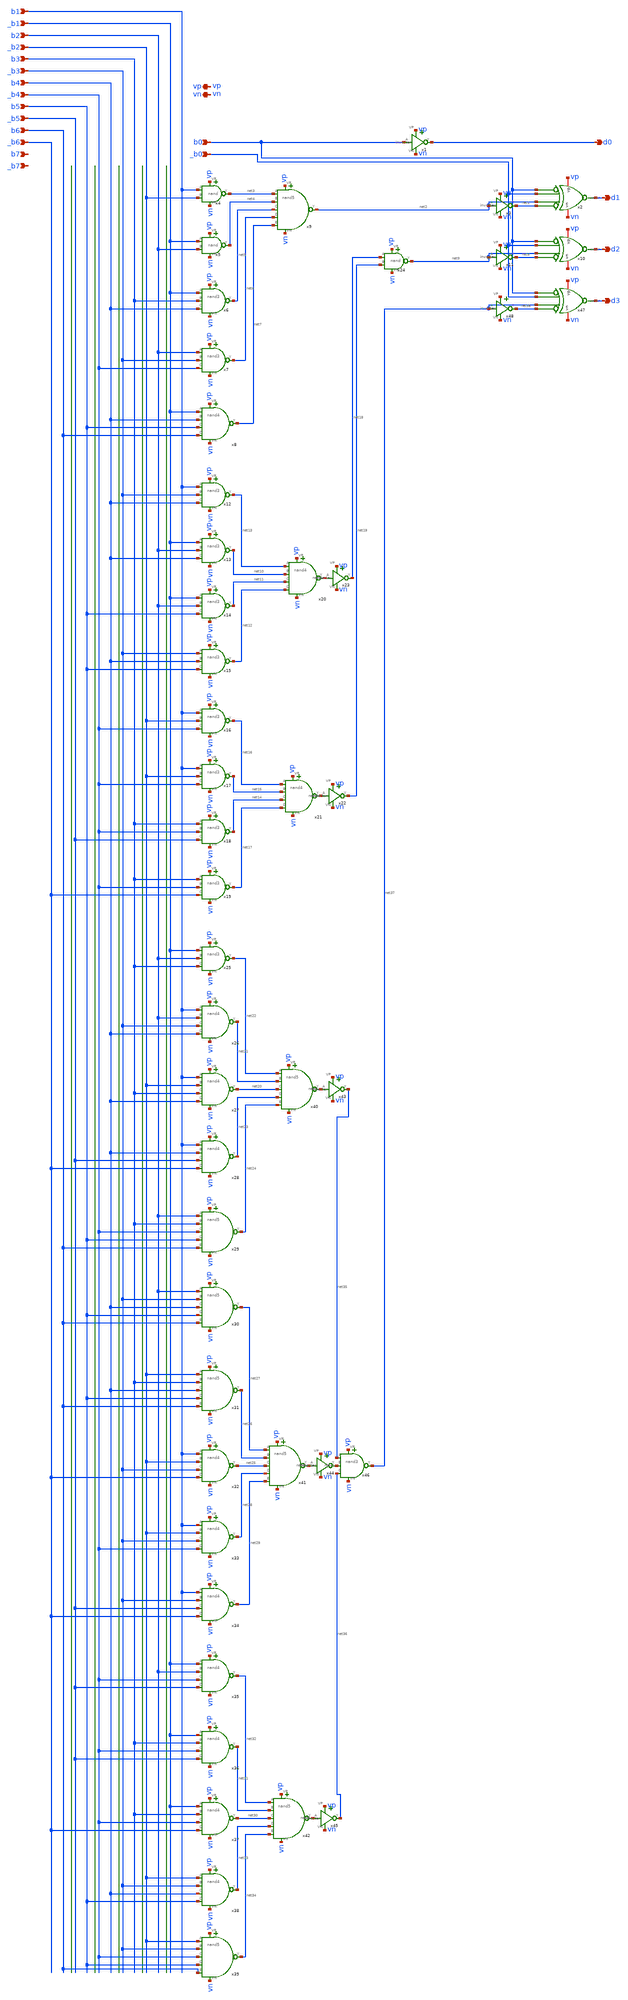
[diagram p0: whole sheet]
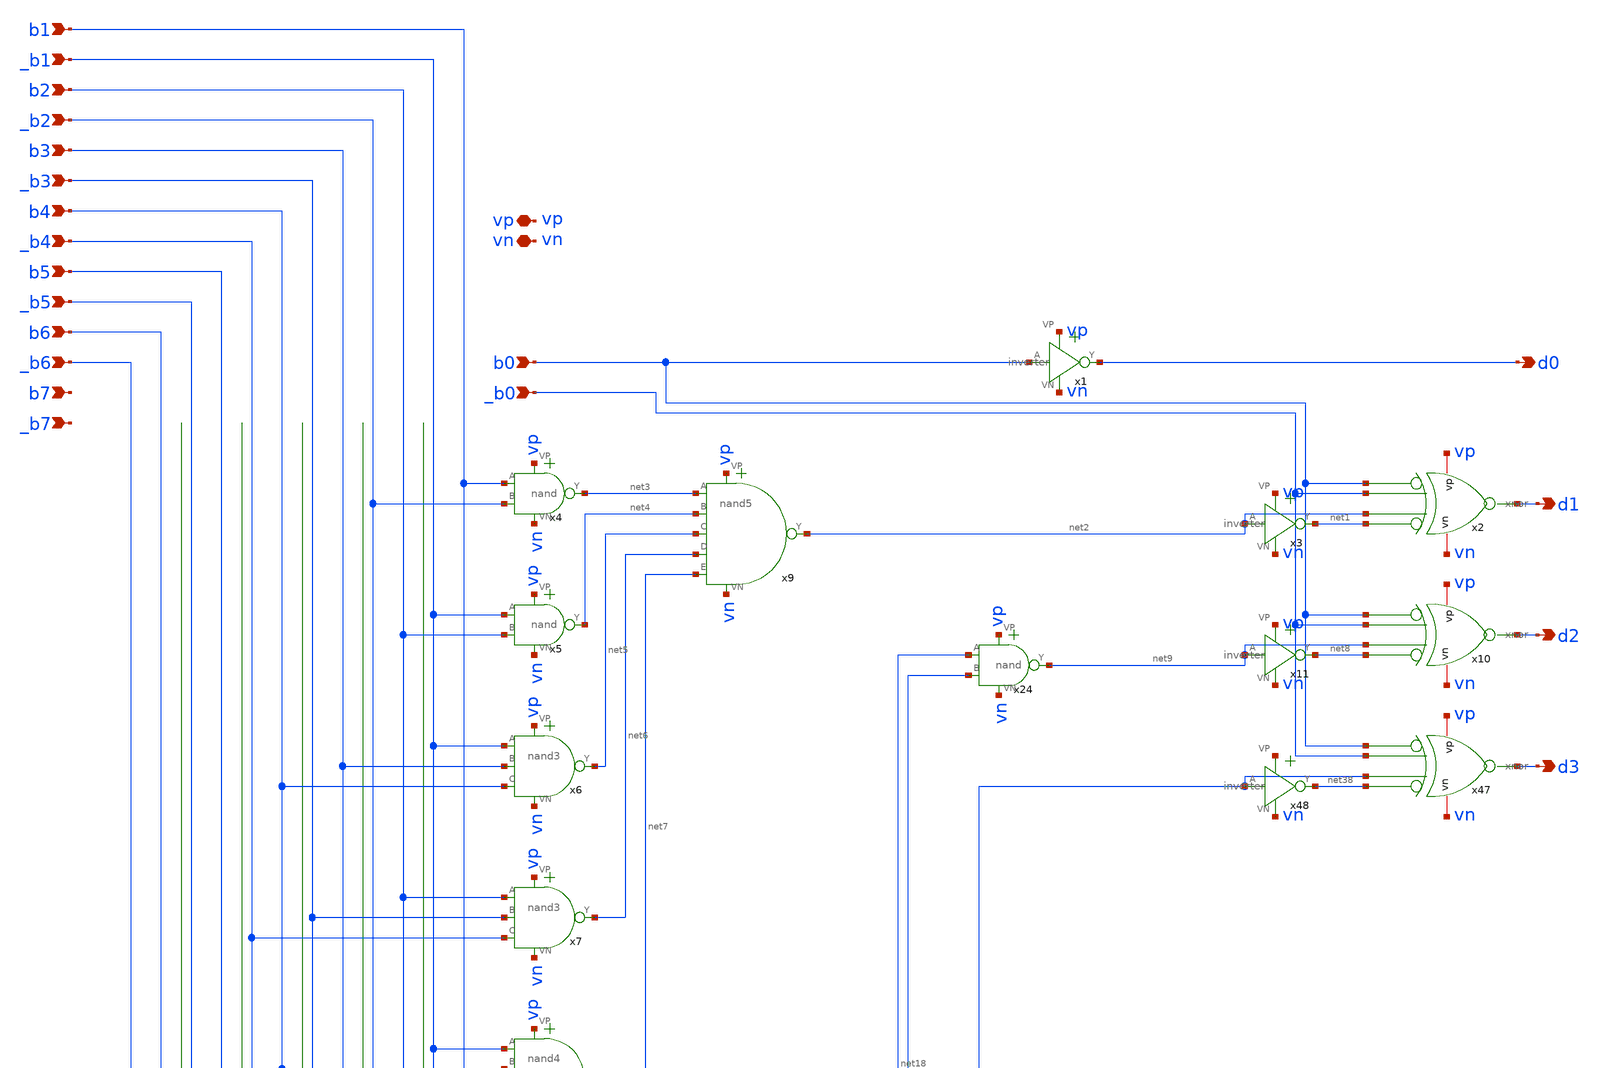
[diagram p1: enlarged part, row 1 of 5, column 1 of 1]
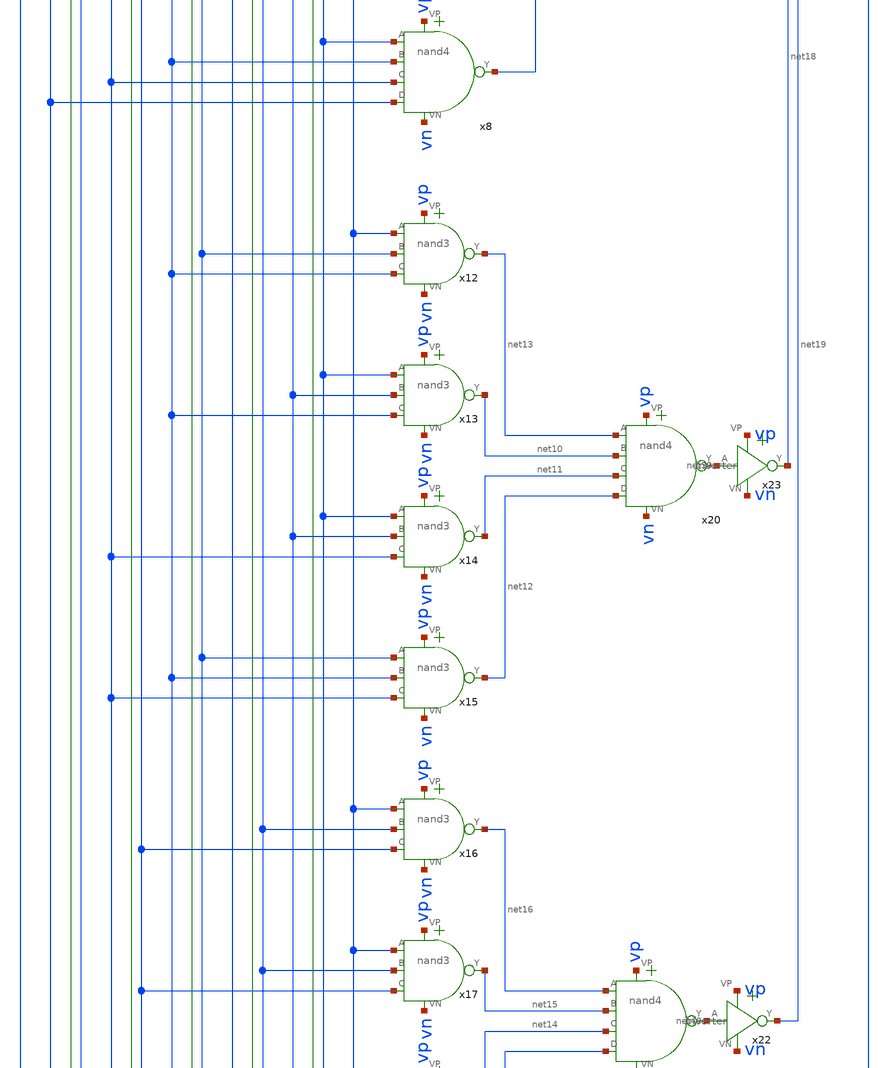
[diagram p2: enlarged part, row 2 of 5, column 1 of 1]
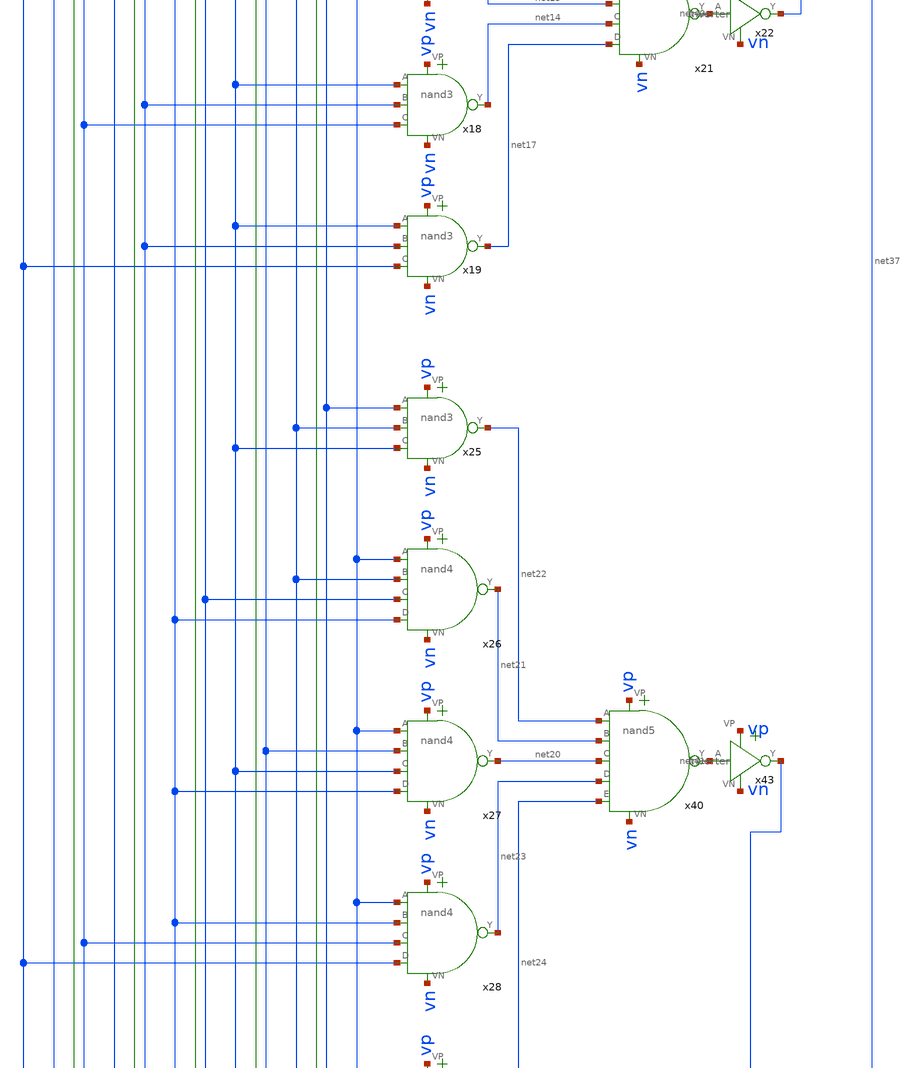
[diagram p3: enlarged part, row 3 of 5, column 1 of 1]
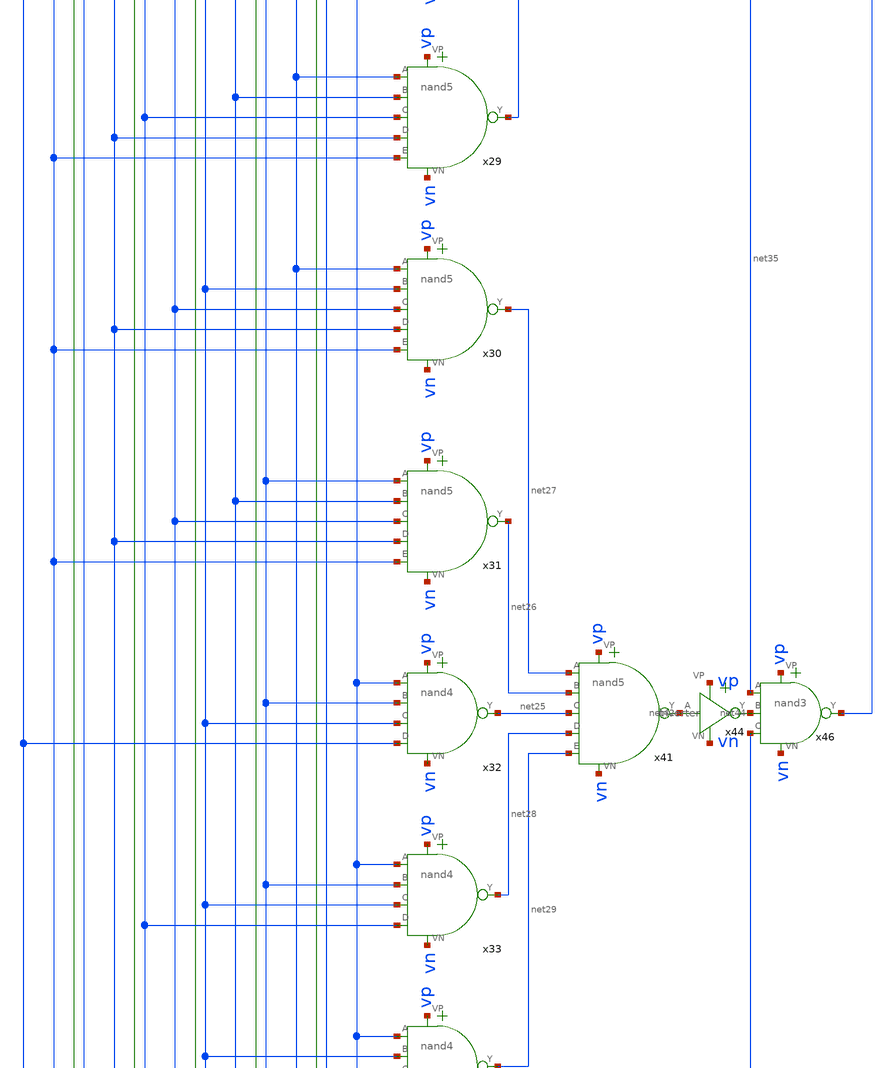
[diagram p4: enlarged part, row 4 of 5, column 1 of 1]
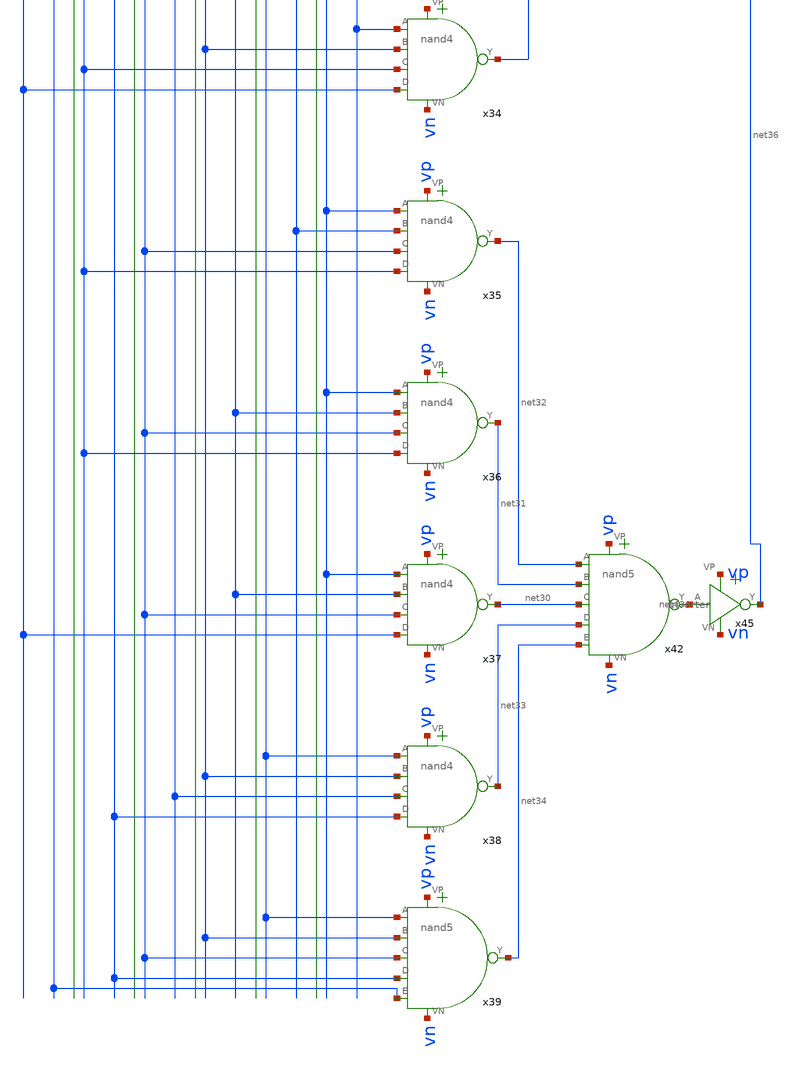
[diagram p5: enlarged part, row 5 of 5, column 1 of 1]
** sch_path: xschem/sin_cl.sch
**.subckt sin_cl _b0 b1 _b1 b2 _b2 b3 _b3 b4 _b4 b5 _b5 b6 _b6 b7 _b7 b0 d0 d1 d2 d3 vp vn
*.ipin _b0
*.ipin b1
*.ipin _b1
*.ipin b2
*.ipin _b2
*.ipin b3
*.ipin _b3
*.ipin b4
*.ipin _b4
*.ipin b5
*.ipin _b5
*.ipin b6
*.ipin _b6
*.ipin b7
*.ipin _b7
*.ipin b0
*.opin d0
*.opin d1
*.opin d2
*.opin d3
*.iopin vp
*.iopin vn
x1 vp b0 d0 vn inverter
x2 vp _b0 net2 d1 b0 net1 vn xnor
x3 vp net2 net1 vn inverter
x4 vn b1 _b2 net3 vp nand
x5 vn _b1 b2 net4 vp nand
x6 vn _b1 b3 net5 vp b4 nand3
x7 vn b2 _b3 net6 vp _b4 nand3
x8 vn _b1 b4 net7 vp b5 b6 nand4
x9 vn net3 net4 net2 vp net5 net6 net7 nand5
x10 vp _b0 net9 d2 b0 net8 vn xnor
x11 vp net9 net8 vn inverter
x12 vn b1 _b3 net13 vp b4 nand3
x13 vn _b1 b2 net10 vp b4 nand3
x14 vn _b1 b2 net11 vp b5 nand3
x15 vn _b3 b4 net12 vp b5 nand3
x16 vn b1 _b2 net16 vp _b4 nand3
x17 vn b1 _b2 net15 vp _b4 nand3
x18 vn b3 _b4 net14 vp _b5 nand3
x19 vn b3 _b4 net17 vp _b6 nand3
x20 vn net13 net10 net39 vp net11 net12 nand4
x21 vn net16 net15 net40 vp net14 net17 nand4
x22 vp net40 net19 vn inverter
x23 vp net39 net18 vn inverter
x24 vn net18 net19 net9 vp nand
x25 vn _b1 b2 net22 vp b3 nand3
x26 vn b1 b2 net21 vp _b3 b4 nand4
x27 vn b1 _b2 net20 vp b3 b4 nand4
x28 vn b1 b4 net23 vp _b5 _b6 nand4
x29 vn b2 b3 net24 vp _b4 b5 b6 nand5
x30 vn b2 _b3 net27 vp b4 b5 b6 nand5
x31 vn _b2 b3 net26 vp b4 b5 b6 nand5
x32 vn b1 _b2 net25 vp _b3 _b6 nand4
x33 vn b1 _b2 net28 vp _b3 _b4 nand4
x34 vn b1 _b3 net29 vp _b5 _b6 nand4
x35 vn _b1 b2 net32 vp _b4 _b5 nand4
x36 vn _b1 b3 net31 vp _b4 _b5 nand4
x37 vn _b1 b3 net30 vp _b4 _b6 nand4
x38 vn _b2 _b3 net33 vp b4 b5 nand4
x39 vn _b2 _b3 net34 vp _b4 b5 b6 nand5
x40 vn net22 net21 net41 vp net20 net23 net24 nand5
x41 vn net27 net26 net42 vp net25 net28 net29 nand5
x42 vn net32 net31 net43 vp net30 net33 net34 nand5
x43 vp net41 net35 vn inverter
x44 vp net42 net44 vn inverter
x45 vp net43 net36 vn inverter
x46 vn net35 net44 net37 vp net36 nand3
x47 vp _b0 net37 d3 b0 net38 vn xnor
x48 net45 net37 net38 vn inverter
**.ends

* expanding   symbol:  /home/madvlsi/dev/git/magic-dds/xschem/other_project_files/inverter.sym # of
*+ pins=4
** sym_path: xschem/other_project_files/inverter.sym
** sch_path: xschem/other_project_files/inverter.sch
.subckt inverter VP A Y VN
*.iopin VP
*.iopin VN
*.ipin A
*.opin Y
XM1 Y A VN VN sky130_fd_pr__nfet_01v8 L=0.15 W=1 nf=1 ad='int((nf+1)/2) * W/nf * 0.29' as='int((nf+2)/2) * W/nf * 0.29'
+ pd='2*int((nf+1)/2) * (W/nf + 0.29)' ps='2*int((nf+2)/2) * (W/nf + 0.29)' nrd='0.29 / W' nrs='0.29 / W'
+ sa=0 sb=0 sd=0 mult=1 m=1
XM2 Y A VP VP sky130_fd_pr__pfet_01v8 L=0.15 W=4 nf=1 ad='int((nf+1)/2) * W/nf * 0.29' as='int((nf+2)/2) * W/nf * 0.29'
+ pd='2*int((nf+1)/2) * (W/nf + 0.29)' ps='2*int((nf+2)/2) * (W/nf + 0.29)' nrd='0.29 / W' nrs='0.29 / W'
+ sa=0 sb=0 sd=0 mult=1 m=1
.ends


* expanding   symbol:  /home/madvlsi/dev/git/magic-dds/xschem/logic_gates/xnor.sym # of pins=7
** sym_path: xschem/logic_gates/xnor.sym
** sch_path: xschem/logic_gates/xnor.sch
.subckt xnor vp A B Y _A _B vn
*.iopin vp
*.iopin vn
*.ipin A
*.ipin B
*.ipin _A
*.ipin _B
*.opin Y
x1 vn A B net1 vp nand
x2 vn _A _B net2 vp nand
x3 vn net1 net2 Y vp nand
.ends


* expanding   symbol:  /home/madvlsi/dev/git/magic-dds/xschem/logic_gates/nand.sym # of pins=5
** sym_path: xschem/logic_gates/nand.sym
** sch_path: xschem/logic_gates/nand.sch
.subckt nand VN A B Y VP
*.iopin VP
*.iopin VN
*.ipin A
*.ipin B
*.opin Y
XM1 Y A net1 GND sky130_fd_pr__nfet_01v8 L=0.15 W=1 nf=1 ad='int((nf+1)/2) * W/nf * 0.29' as='int((nf+2)/2) * W/nf * 0.29'
+ pd='2*int((nf+1)/2) * (W/nf + 0.29)' ps='2*int((nf+2)/2) * (W/nf + 0.29)' nrd='0.29 / W' nrs='0.29 / W'
+ sa=0 sb=0 sd=0 mult=1 m=1
XM2 net1 B VN GND sky130_fd_pr__nfet_01v8 L=0.15 W=1 nf=1 ad='int((nf+1)/2) * W/nf * 0.29' as='int((nf+2)/2) * W/nf * 0.29'
+ pd='2*int((nf+1)/2) * (W/nf + 0.29)' ps='2*int((nf+2)/2) * (W/nf + 0.29)' nrd='0.29 / W' nrs='0.29 / W'
+ sa=0 sb=0 sd=0 mult=1 m=1
XM3 Y A VP VDD sky130_fd_pr__pfet_01v8 L=0.15 W=1 nf=1 ad='int((nf+1)/2) * W/nf * 0.29' as='int((nf+2)/2) * W/nf * 0.29'
+ pd='2*int((nf+1)/2) * (W/nf + 0.29)' ps='2*int((nf+2)/2) * (W/nf + 0.29)' nrd='0.29 / W' nrs='0.29 / W'
+ sa=0 sb=0 sd=0 mult=1 m=1
XM4 Y B VP VDD sky130_fd_pr__pfet_01v8 L=0.15 W=1 nf=1 ad='int((nf+1)/2) * W/nf * 0.29' as='int((nf+2)/2) * W/nf * 0.29'
+ pd='2*int((nf+1)/2) * (W/nf + 0.29)' ps='2*int((nf+2)/2) * (W/nf + 0.29)' nrd='0.29 / W' nrs='0.29 / W'
+ sa=0 sb=0 sd=0 mult=1 m=1
.ends


* expanding   symbol:  /home/madvlsi/dev/git/magic-dds/xschem/logic_gates/nand3.sym # of pins=6
** sym_path: xschem/logic_gates/nand3.sym
** sch_path: xschem/logic_gates/nand3.sch
.subckt nand3 VN A B Y VP C
*.iopin VP
*.iopin VN
*.ipin A
*.ipin B
*.opin Y
*.ipin C
XM1 Y A net1 GND sky130_fd_pr__nfet_01v8 L=0.15 W=1 nf=1 ad='int((nf+1)/2) * W/nf * 0.29' as='int((nf+2)/2) * W/nf * 0.29'
+ pd='2*int((nf+1)/2) * (W/nf + 0.29)' ps='2*int((nf+2)/2) * (W/nf + 0.29)' nrd='0.29 / W' nrs='0.29 / W'
+ sa=0 sb=0 sd=0 mult=1 m=1
XM2 net1 B net2 GND sky130_fd_pr__nfet_01v8 L=0.15 W=1 nf=1 ad='int((nf+1)/2) * W/nf * 0.29' as='int((nf+2)/2) * W/nf * 0.29'
+ pd='2*int((nf+1)/2) * (W/nf + 0.29)' ps='2*int((nf+2)/2) * (W/nf + 0.29)' nrd='0.29 / W' nrs='0.29 / W'
+ sa=0 sb=0 sd=0 mult=1 m=1
XM3 Y A VP VDD sky130_fd_pr__pfet_01v8 L=0.15 W=1 nf=1 ad='int((nf+1)/2) * W/nf * 0.29' as='int((nf+2)/2) * W/nf * 0.29'
+ pd='2*int((nf+1)/2) * (W/nf + 0.29)' ps='2*int((nf+2)/2) * (W/nf + 0.29)' nrd='0.29 / W' nrs='0.29 / W'
+ sa=0 sb=0 sd=0 mult=1 m=1
XM4 Y B VP VDD sky130_fd_pr__pfet_01v8 L=0.15 W=1 nf=1 ad='int((nf+1)/2) * W/nf * 0.29' as='int((nf+2)/2) * W/nf * 0.29'
+ pd='2*int((nf+1)/2) * (W/nf + 0.29)' ps='2*int((nf+2)/2) * (W/nf + 0.29)' nrd='0.29 / W' nrs='0.29 / W'
+ sa=0 sb=0 sd=0 mult=1 m=1
XM5 net2 C VN GND sky130_fd_pr__nfet_01v8 L=0.15 W=1 nf=1 ad='int((nf+1)/2) * W/nf * 0.29' as='int((nf+2)/2) * W/nf * 0.29'
+ pd='2*int((nf+1)/2) * (W/nf + 0.29)' ps='2*int((nf+2)/2) * (W/nf + 0.29)' nrd='0.29 / W' nrs='0.29 / W'
+ sa=0 sb=0 sd=0 mult=1 m=1
XM6 Y C VP VDD sky130_fd_pr__pfet_01v8 L=0.15 W=1 nf=1 ad='int((nf+1)/2) * W/nf * 0.29' as='int((nf+2)/2) * W/nf * 0.29'
+ pd='2*int((nf+1)/2) * (W/nf + 0.29)' ps='2*int((nf+2)/2) * (W/nf + 0.29)' nrd='0.29 / W' nrs='0.29 / W'
+ sa=0 sb=0 sd=0 mult=1 m=1
.ends


* expanding   symbol:  /home/madvlsi/dev/git/magic-dds/xschem/logic_gates/nand4.sym # of pins=7
** sym_path: xschem/logic_gates/nand4.sym
** sch_path: xschem/logic_gates/nand4.sch
.subckt nand4 VN A B Y VP C D
*.iopin VP
*.iopin VN
*.ipin A
*.ipin B
*.opin Y
*.ipin C
*.ipin D
XM1 Y A net1 GND sky130_fd_pr__nfet_01v8 L=0.15 W=1 nf=1 ad='int((nf+1)/2) * W/nf * 0.29' as='int((nf+2)/2) * W/nf * 0.29'
+ pd='2*int((nf+1)/2) * (W/nf + 0.29)' ps='2*int((nf+2)/2) * (W/nf + 0.29)' nrd='0.29 / W' nrs='0.29 / W'
+ sa=0 sb=0 sd=0 mult=1 m=1
XM2 net1 B net2 GND sky130_fd_pr__nfet_01v8 L=0.15 W=1 nf=1 ad='int((nf+1)/2) * W/nf * 0.29' as='int((nf+2)/2) * W/nf * 0.29'
+ pd='2*int((nf+1)/2) * (W/nf + 0.29)' ps='2*int((nf+2)/2) * (W/nf + 0.29)' nrd='0.29 / W' nrs='0.29 / W'
+ sa=0 sb=0 sd=0 mult=1 m=1
XM3 Y A VP VDD sky130_fd_pr__pfet_01v8 L=0.15 W=1 nf=1 ad='int((nf+1)/2) * W/nf * 0.29' as='int((nf+2)/2) * W/nf * 0.29'
+ pd='2*int((nf+1)/2) * (W/nf + 0.29)' ps='2*int((nf+2)/2) * (W/nf + 0.29)' nrd='0.29 / W' nrs='0.29 / W'
+ sa=0 sb=0 sd=0 mult=1 m=1
XM4 Y B VP VDD sky130_fd_pr__pfet_01v8 L=0.15 W=1 nf=1 ad='int((nf+1)/2) * W/nf * 0.29' as='int((nf+2)/2) * W/nf * 0.29'
+ pd='2*int((nf+1)/2) * (W/nf + 0.29)' ps='2*int((nf+2)/2) * (W/nf + 0.29)' nrd='0.29 / W' nrs='0.29 / W'
+ sa=0 sb=0 sd=0 mult=1 m=1
XM5 net2 C net3 GND sky130_fd_pr__nfet_01v8 L=0.15 W=1 nf=1 ad='int((nf+1)/2) * W/nf * 0.29' as='int((nf+2)/2) * W/nf * 0.29'
+ pd='2*int((nf+1)/2) * (W/nf + 0.29)' ps='2*int((nf+2)/2) * (W/nf + 0.29)' nrd='0.29 / W' nrs='0.29 / W'
+ sa=0 sb=0 sd=0 mult=1 m=1
XM6 Y C VP VDD sky130_fd_pr__pfet_01v8 L=0.15 W=1 nf=1 ad='int((nf+1)/2) * W/nf * 0.29' as='int((nf+2)/2) * W/nf * 0.29'
+ pd='2*int((nf+1)/2) * (W/nf + 0.29)' ps='2*int((nf+2)/2) * (W/nf + 0.29)' nrd='0.29 / W' nrs='0.29 / W'
+ sa=0 sb=0 sd=0 mult=1 m=1
XM7 Y D VP VDD sky130_fd_pr__pfet_01v8 L=0.15 W=1 nf=1 ad='int((nf+1)/2) * W/nf * 0.29' as='int((nf+2)/2) * W/nf * 0.29'
+ pd='2*int((nf+1)/2) * (W/nf + 0.29)' ps='2*int((nf+2)/2) * (W/nf + 0.29)' nrd='0.29 / W' nrs='0.29 / W'
+ sa=0 sb=0 sd=0 mult=1 m=1
XM8 net3 D VN GND sky130_fd_pr__nfet_01v8 L=0.15 W=1 nf=1 ad='int((nf+1)/2) * W/nf * 0.29' as='int((nf+2)/2) * W/nf * 0.29'
+ pd='2*int((nf+1)/2) * (W/nf + 0.29)' ps='2*int((nf+2)/2) * (W/nf + 0.29)' nrd='0.29 / W' nrs='0.29 / W'
+ sa=0 sb=0 sd=0 mult=1 m=1
.ends


* expanding   symbol:  /home/madvlsi/dev/git/magic-dds/xschem/logic_gates/nand5.sym # of pins=8
** sym_path: xschem/logic_gates/nand5.sym
** sch_path: xschem/logic_gates/nand5.sch
.subckt nand5 VN A B Y VP C D E
*.iopin VP
*.iopin VN
*.ipin A
*.ipin B
*.opin Y
*.ipin C
*.ipin D
*.ipin E
XM1 Y A net1 GND sky130_fd_pr__nfet_01v8 L=0.15 W=1 nf=1 ad='int((nf+1)/2) * W/nf * 0.29' as='int((nf+2)/2) * W/nf * 0.29'
+ pd='2*int((nf+1)/2) * (W/nf + 0.29)' ps='2*int((nf+2)/2) * (W/nf + 0.29)' nrd='0.29 / W' nrs='0.29 / W'
+ sa=0 sb=0 sd=0 mult=1 m=1
XM2 net1 B net2 GND sky130_fd_pr__nfet_01v8 L=0.15 W=1 nf=1 ad='int((nf+1)/2) * W/nf * 0.29' as='int((nf+2)/2) * W/nf * 0.29'
+ pd='2*int((nf+1)/2) * (W/nf + 0.29)' ps='2*int((nf+2)/2) * (W/nf + 0.29)' nrd='0.29 / W' nrs='0.29 / W'
+ sa=0 sb=0 sd=0 mult=1 m=1
XM3 Y A VP VDD sky130_fd_pr__pfet_01v8 L=0.15 W=1 nf=1 ad='int((nf+1)/2) * W/nf * 0.29' as='int((nf+2)/2) * W/nf * 0.29'
+ pd='2*int((nf+1)/2) * (W/nf + 0.29)' ps='2*int((nf+2)/2) * (W/nf + 0.29)' nrd='0.29 / W' nrs='0.29 / W'
+ sa=0 sb=0 sd=0 mult=1 m=1
XM4 Y B VP VDD sky130_fd_pr__pfet_01v8 L=0.15 W=1 nf=1 ad='int((nf+1)/2) * W/nf * 0.29' as='int((nf+2)/2) * W/nf * 0.29'
+ pd='2*int((nf+1)/2) * (W/nf + 0.29)' ps='2*int((nf+2)/2) * (W/nf + 0.29)' nrd='0.29 / W' nrs='0.29 / W'
+ sa=0 sb=0 sd=0 mult=1 m=1
XM5 net2 C net3 GND sky130_fd_pr__nfet_01v8 L=0.15 W=1 nf=1 ad='int((nf+1)/2) * W/nf * 0.29' as='int((nf+2)/2) * W/nf * 0.29'
+ pd='2*int((nf+1)/2) * (W/nf + 0.29)' ps='2*int((nf+2)/2) * (W/nf + 0.29)' nrd='0.29 / W' nrs='0.29 / W'
+ sa=0 sb=0 sd=0 mult=1 m=1
XM6 Y C VP VDD sky130_fd_pr__pfet_01v8 L=0.15 W=1 nf=1 ad='int((nf+1)/2) * W/nf * 0.29' as='int((nf+2)/2) * W/nf * 0.29'
+ pd='2*int((nf+1)/2) * (W/nf + 0.29)' ps='2*int((nf+2)/2) * (W/nf + 0.29)' nrd='0.29 / W' nrs='0.29 / W'
+ sa=0 sb=0 sd=0 mult=1 m=1
XM7 Y D VP VDD sky130_fd_pr__pfet_01v8 L=0.15 W=1 nf=1 ad='int((nf+1)/2) * W/nf * 0.29' as='int((nf+2)/2) * W/nf * 0.29'
+ pd='2*int((nf+1)/2) * (W/nf + 0.29)' ps='2*int((nf+2)/2) * (W/nf + 0.29)' nrd='0.29 / W' nrs='0.29 / W'
+ sa=0 sb=0 sd=0 mult=1 m=1
XM8 net3 D net4 GND sky130_fd_pr__nfet_01v8 L=0.15 W=1 nf=1 ad='int((nf+1)/2) * W/nf * 0.29' as='int((nf+2)/2) * W/nf * 0.29'
+ pd='2*int((nf+1)/2) * (W/nf + 0.29)' ps='2*int((nf+2)/2) * (W/nf + 0.29)' nrd='0.29 / W' nrs='0.29 / W'
+ sa=0 sb=0 sd=0 mult=1 m=1
XM9 Y E VP VDD sky130_fd_pr__pfet_01v8 L=0.15 W=1 nf=1 ad='int((nf+1)/2) * W/nf * 0.29' as='int((nf+2)/2) * W/nf * 0.29'
+ pd='2*int((nf+1)/2) * (W/nf + 0.29)' ps='2*int((nf+2)/2) * (W/nf + 0.29)' nrd='0.29 / W' nrs='0.29 / W'
+ sa=0 sb=0 sd=0 mult=1 m=1
XM10 net4 E VN GND sky130_fd_pr__nfet_01v8 L=0.15 W=1 nf=1 ad='int((nf+1)/2) * W/nf * 0.29' as='int((nf+2)/2) * W/nf * 0.29'
+ pd='2*int((nf+1)/2) * (W/nf + 0.29)' ps='2*int((nf+2)/2) * (W/nf + 0.29)' nrd='0.29 / W' nrs='0.29 / W'
+ sa=0 sb=0 sd=0 mult=1 m=1
.ends

.end
